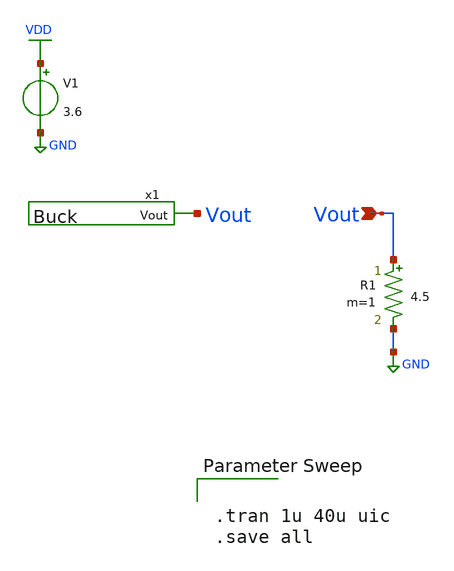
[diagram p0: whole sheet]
** sch_path: Ene_Thompson/test_Buck.sch
**.subckt test_Buck Vout
*.ipin Vout
x1 Vout Buck
V1 VDD GND 3.6
R1 Vout GND 4.5 m=1
**** begin user architecture code

.lib $::SKYWATER_MODELS/sky130.lib.spice tt



.tran 1u 40u uic
.save all


**** end user architecture code
**.ends

* expanding   symbol:  Buck.sym # of pins=1
** sym_path: Ene_Thompson/Buck.sym
** sch_path: Ene_Thompson/Buck.sch
.subckt Buck Vout
*.opin Vout
XM1 vl pswitch VDD VDD sky130_fd_pr__pfet_g5v0d10v5 L=0.5 W=20 nf=1 ad='int((nf+1)/2) * W/nf * 0.29'
+ as='int((nf+2)/2) * W/nf * 0.29' pd='2*int((nf+1)/2) * (W/nf + 0.29)' ps='2*int((nf+2)/2) * (W/nf + 0.29)'
+ nrd='0.29 / W' nrs='0.29 / W' sa=0 sb=0 sd=0 mult=1000 m=1000
XM2 vl nswitch GND GND sky130_fd_pr__nfet_g5v0d10v5 L=0.5 W=20 nf=1 ad='int((nf+1)/2) * W/nf * 0.29'
+ as='int((nf+2)/2) * W/nf * 0.29' pd='2*int((nf+1)/2) * (W/nf + 0.29)' ps='2*int((nf+2)/2) * (W/nf + 0.29)'
+ nrd='0.29 / W' nrs='0.29 / W' sa=0 sb=0 sd=0 mult=1000 m=1000
L1 net2 Vout 4.7u m=1
C1 Vout net1 1u m=1
V1 pswitch GND PULSE(0 5 0 0.01u 0.01u 0.5u 1u)
R1 vl net2 1.5m m=1
R2 GND net1 10m m=1
V2 nswitch GND PULSE(0 5 50n 0.01u 0.01u 0.55u 1u)
.ends

.GLOBAL VDD
.GLOBAL GND
.end
